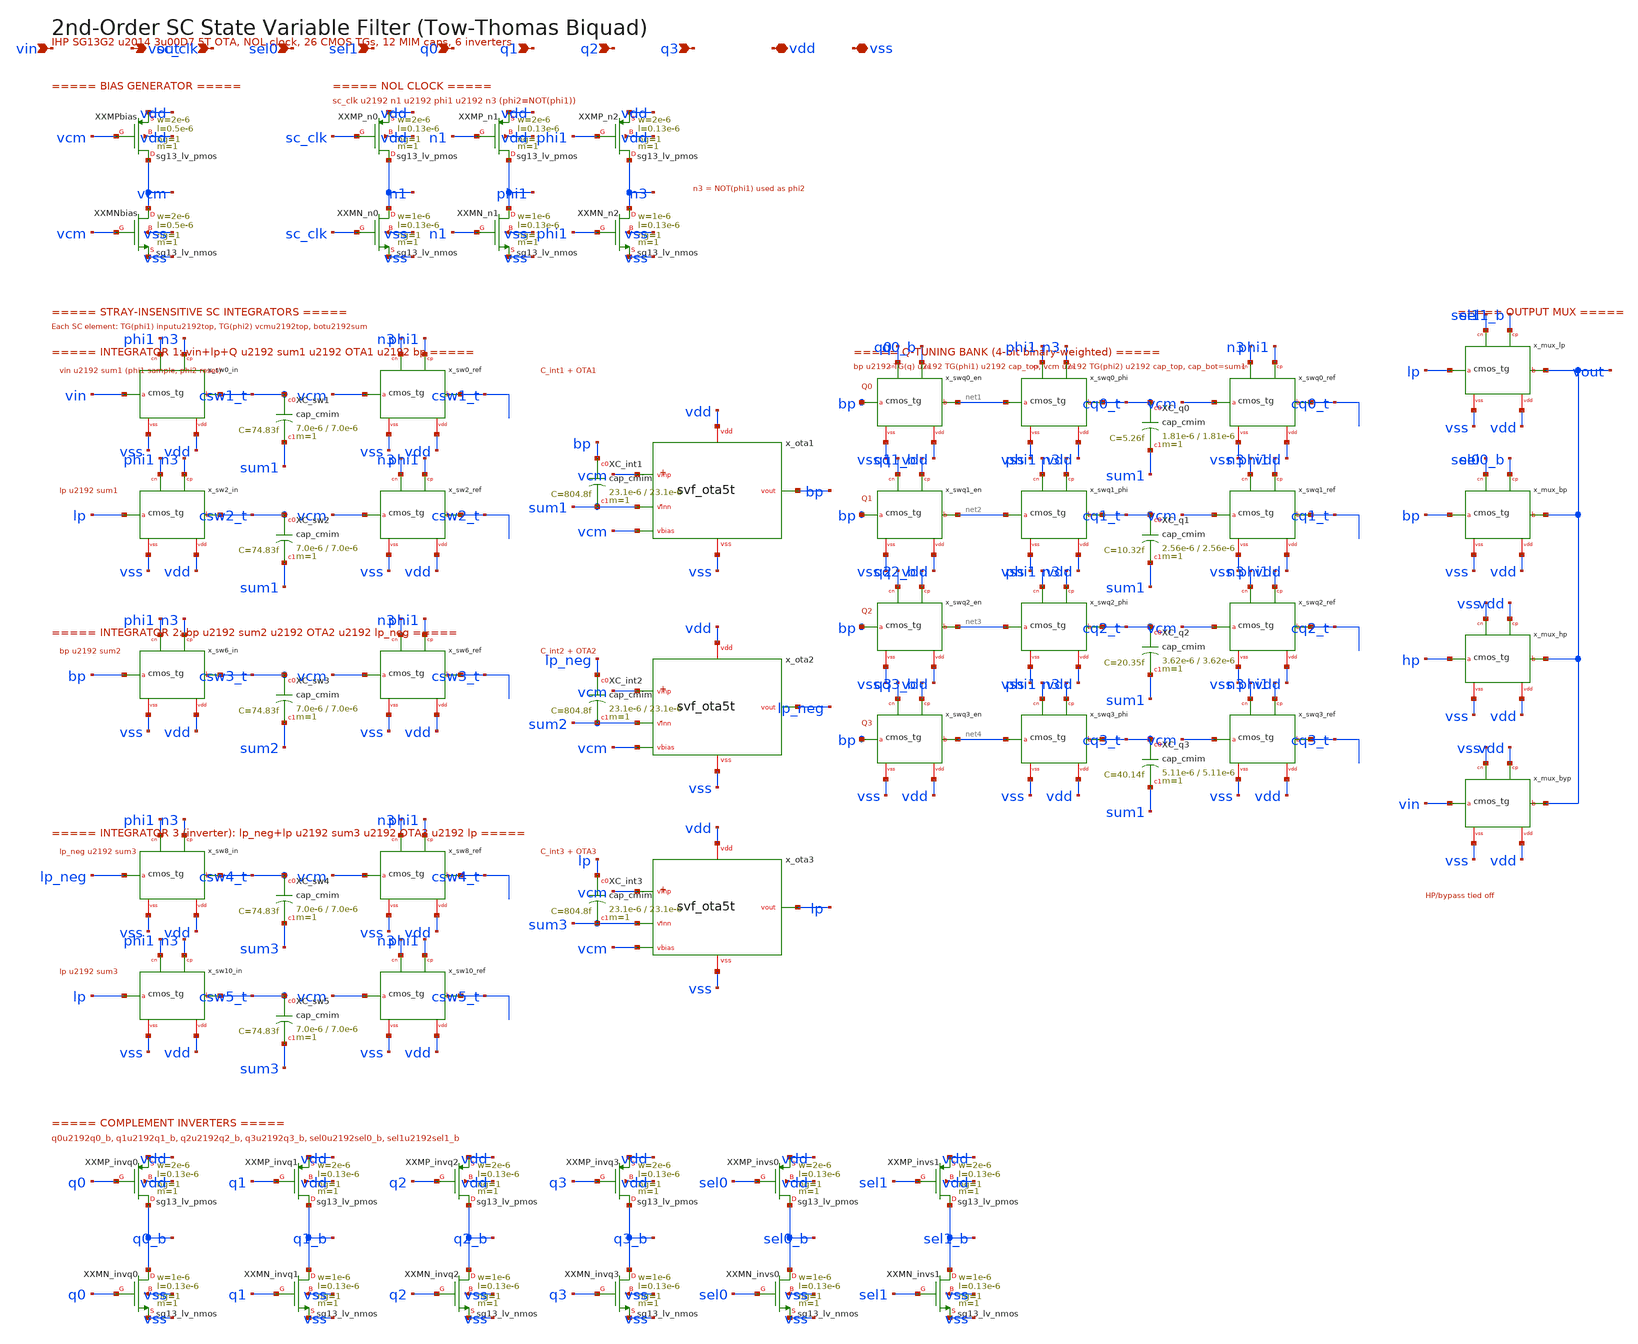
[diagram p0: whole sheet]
** sch_path: xschem/svf_2nd.sch
**.subckt svf_2nd vin vout sc_clk sel0 sel1 q0 q1 q2 q3 vdd vss
*.ipin vin
*.opin vout
*.ipin sc_clk
*.ipin sel0
*.ipin sel1
*.ipin q0
*.ipin q1
*.ipin q2
*.ipin q3
*.iopin vdd
*.iopin vss
XXXMPbias vcm vcm vdd vdd sg13_lv_pmos w=2e-6 l=0.5e-6 ng=1 m=1 mm_ok=1
XXXMNbias vcm vcm vss vss sg13_lv_nmos w=2e-6 l=0.5e-6 ng=1 m=1 mm_ok=1
XXXMP_n0 n1 sc_clk vdd vdd sg13_lv_pmos w=2e-6 l=0.13e-6 ng=1 m=1 mm_ok=1
XXXMN_n0 n1 sc_clk vss vss sg13_lv_nmos w=1e-6 l=0.13e-6 ng=1 m=1 mm_ok=1
XXXMP_n1 phi1 n1 vdd vdd sg13_lv_pmos w=2e-6 l=0.13e-6 ng=1 m=1 mm_ok=1
XXXMN_n1 phi1 n1 vss vss sg13_lv_nmos w=1e-6 l=0.13e-6 ng=1 m=1 mm_ok=1
XXXMP_n2 n3 phi1 vdd vdd sg13_lv_pmos w=2e-6 l=0.13e-6 ng=1 m=1 mm_ok=1
XXXMN_n2 n3 phi1 vss vss sg13_lv_nmos w=1e-6 l=0.13e-6 ng=1 m=1 mm_ok=1
x_sw0_in vin csw1_t phi1 n3 vss vdd cmos_tg
x_sw0_ref vcm csw1_t n3 phi1 vss vdd cmos_tg
XXC_sw1 csw1_t sum1 cap_cmim w=7.0e-6 l=7.0e-6 m=1 mm_ok=1
x_sw2_in lp csw2_t phi1 n3 vss vdd cmos_tg
x_sw2_ref vcm csw2_t n3 phi1 vss vdd cmos_tg
XXC_sw2 csw2_t sum1 cap_cmim w=7.0e-6 l=7.0e-6 m=1 mm_ok=1
XXC_int1 bp sum1 cap_cmim w=23.1e-6 l=23.1e-6 m=1 mm_ok=1
x_ota1 vcm sum1 vcm bp vdd vss svf_ota5t
x_sw6_in bp csw3_t phi1 n3 vss vdd cmos_tg
x_sw6_ref vcm csw3_t n3 phi1 vss vdd cmos_tg
XXC_sw3 csw3_t sum2 cap_cmim w=7.0e-6 l=7.0e-6 m=1 mm_ok=1
XXC_int2 lp_neg sum2 cap_cmim w=23.1e-6 l=23.1e-6 m=1 mm_ok=1
x_ota2 vcm sum2 vcm lp_neg vdd vss svf_ota5t
x_sw8_in lp_neg csw4_t phi1 n3 vss vdd cmos_tg
x_sw8_ref vcm csw4_t n3 phi1 vss vdd cmos_tg
XXC_sw4 csw4_t sum3 cap_cmim w=7.0e-6 l=7.0e-6 m=1 mm_ok=1
x_sw10_in lp csw5_t phi1 n3 vss vdd cmos_tg
x_sw10_ref vcm csw5_t n3 phi1 vss vdd cmos_tg
XXC_sw5 csw5_t sum3 cap_cmim w=7.0e-6 l=7.0e-6 m=1 mm_ok=1
XXC_int3 lp sum3 cap_cmim w=23.1e-6 l=23.1e-6 m=1 mm_ok=1
x_ota3 vcm sum3 vcm lp vdd vss svf_ota5t
x_swq0_en bp net1 q0 q0_b vss vdd cmos_tg
x_swq0_phi net1 cq0_t phi1 n3 vss vdd cmos_tg
x_swq0_ref vcm cq0_t n3 phi1 vss vdd cmos_tg
XXC_q0 cq0_t sum1 cap_cmim w=1.81e-6 l=1.81e-6 m=1 mm_ok=1
x_swq1_en bp net2 q1 q1_b vss vdd cmos_tg
x_swq1_phi net2 cq1_t phi1 n3 vss vdd cmos_tg
x_swq1_ref vcm cq1_t n3 phi1 vss vdd cmos_tg
XXC_q1 cq1_t sum1 cap_cmim w=2.56e-6 l=2.56e-6 m=1 mm_ok=1
x_swq2_en bp net3 q2 q2_b vss vdd cmos_tg
x_swq2_phi net3 cq2_t phi1 n3 vss vdd cmos_tg
x_swq2_ref vcm cq2_t n3 phi1 vss vdd cmos_tg
XXC_q2 cq2_t sum1 cap_cmim w=3.62e-6 l=3.62e-6 m=1 mm_ok=1
x_swq3_en bp net4 q3 q3_b vss vdd cmos_tg
x_swq3_phi net4 cq3_t phi1 n3 vss vdd cmos_tg
x_swq3_ref vcm cq3_t n3 phi1 vss vdd cmos_tg
XXC_q3 cq3_t sum1 cap_cmim w=5.11e-6 l=5.11e-6 m=1 mm_ok=1
x_mux_lp lp vout sel1 sel1_b vss vdd cmos_tg
x_mux_bp bp vout sel0 sel0_b vss vdd cmos_tg
x_mux_hp hp vout vss vdd vss vdd cmos_tg
x_mux_byp vin vout vss vdd vss vdd cmos_tg
XXXMP_invq0 q0_b q0 vdd vdd sg13_lv_pmos w=2e-6 l=0.13e-6 ng=1 m=1 mm_ok=1
XXXMN_invq0 q0_b q0 vss vss sg13_lv_nmos w=1e-6 l=0.13e-6 ng=1 m=1 mm_ok=1
XXXMP_invq1 q1_b q1 vdd vdd sg13_lv_pmos w=2e-6 l=0.13e-6 ng=1 m=1 mm_ok=1
XXXMN_invq1 q1_b q1 vss vss sg13_lv_nmos w=1e-6 l=0.13e-6 ng=1 m=1 mm_ok=1
XXXMP_invq2 q2_b q2 vdd vdd sg13_lv_pmos w=2e-6 l=0.13e-6 ng=1 m=1 mm_ok=1
XXXMN_invq2 q2_b q2 vss vss sg13_lv_nmos w=1e-6 l=0.13e-6 ng=1 m=1 mm_ok=1
XXXMP_invq3 q3_b q3 vdd vdd sg13_lv_pmos w=2e-6 l=0.13e-6 ng=1 m=1 mm_ok=1
XXXMN_invq3 q3_b q3 vss vss sg13_lv_nmos w=1e-6 l=0.13e-6 ng=1 m=1 mm_ok=1
XXXMP_invs0 sel0_b sel0 vdd vdd sg13_lv_pmos w=2e-6 l=0.13e-6 ng=1 m=1 mm_ok=1
XXXMN_invs0 sel0_b sel0 vss vss sg13_lv_nmos w=1e-6 l=0.13e-6 ng=1 m=1 mm_ok=1
XXXMP_invs1 sel1_b sel1 vdd vdd sg13_lv_pmos w=2e-6 l=0.13e-6 ng=1 m=1 mm_ok=1
XXXMN_invs1 sel1_b sel1 vss vss sg13_lv_nmos w=1e-6 l=0.13e-6 ng=1 m=1 mm_ok=1
**.ends

* expanding   symbol:  cmos_tg.sym # of pins=6
** sym_path: xschem/cmos_tg.sym
** sch_path: xschem/cmos_tg.sch
.subckt cmos_tg a b ctrl_n ctrl_p vss vdd
*.iopin a
*.iopin b
*.ipin ctrl_p
*.iopin vss
*.iopin vdd
*.ipin ctrl_n
XXMN a ctrl_n b vss sg13_lv_nmos w=2e-6 l=0.13e-6 ng=1 m=1 mm_ok=1
XXMP b ctrl_p a vdd sg13_lv_pmos w=4e-6 l=0.13e-6 ng=1 m=1 mm_ok=1
.ends


* expanding   symbol:  svf_ota5t.sym # of pins=6
** sym_path: xschem/svf_ota5t.sym
** sch_path: xschem/svf_ota5t.sch
.subckt svf_ota5t vinp vinn vbias vout vdd vss
*.iopin vdd
*.iopin vss
*.ipin vinp
*.ipin vinn
*.opin vout
*.ipin vbias
XXM3 mirr mirr vdd vdd sg13_lv_pmos w=2e-6 l=0.5e-6 ng=1 m=1 mm_ok=1
XXM4 vout mirr vdd vdd sg13_lv_pmos w=2e-6 l=0.5e-6 ng=1 m=1 mm_ok=1
XXM1 mirr vinp tail vss sg13_lv_nmos w=4e-6 l=0.5e-6 ng=1 m=1 mm_ok=1
XXM2 vout vinn tail vss sg13_lv_nmos w=4e-6 l=0.5e-6 ng=1 m=1 mm_ok=1
XXM5 tail vbias vss vss sg13_lv_nmos w=2e-6 l=0.5e-6 ng=1 m=1 mm_ok=1
.ends

.end
